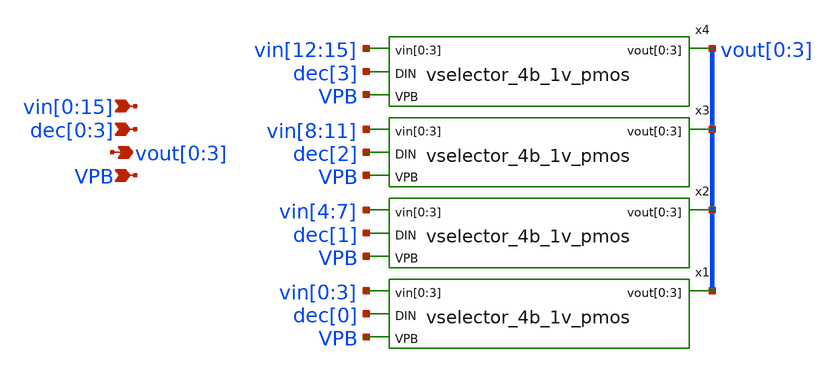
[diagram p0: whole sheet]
** sch_path: xschem/vselector_6b_1v_stage_2_pmos.sch
**.subckt vselector_6b_1v_stage_2_pmos
*+ vin[0],vin[1],vin[2],vin[3],vin[4],vin[5],vin[6],vin[7],vin[8],vin[9],vin[10],vin[11],vin[12],vin[13],vin[14],vin[15] vout[0],vout[1],vout[2],vout[3] VPB dec[0],dec[1],dec[2],dec[3]
*.ipin
*+ vin[0],vin[1],vin[2],vin[3],vin[4],vin[5],vin[6],vin[7],vin[8],vin[9],vin[10],vin[11],vin[12],vin[13],vin[14],vin[15]
*.opin vout[0],vout[1],vout[2],vout[3]
*.ipin VPB
*.ipin dec[0],dec[1],dec[2],dec[3]
x1 vin[0] vin[1] vin[2] vin[3] dec[0] vout[0] vout[1] vout[2] vout[3] VPB vselector_4b_1v_pmos
x2 vin[4] vin[5] vin[6] vin[7] dec[1] vout[0] vout[1] vout[2] vout[3] VPB vselector_4b_1v_pmos
x3 vin[8] vin[9] vin[10] vin[11] dec[2] vout[0] vout[1] vout[2] vout[3] VPB vselector_4b_1v_pmos
x4 vin[12] vin[13] vin[14] vin[15] dec[3] vout[0] vout[1] vout[2] vout[3] VPB vselector_4b_1v_pmos
**.ends

* expanding   symbol:  vselector_4b_1v_pmos.sym # of pins=4
** sym_path: xschem/vselector_4b_1v_pmos.sym
** sch_path: xschem/vselector_4b_1v_pmos.sch
.subckt vselector_4b_1v_pmos vin[0] vin[1] vin[2] vin[3] DIN vout[0] vout[1] vout[2] vout[3] VPB
*.ipin vin[0],vin[1],vin[2],vin[3]
*.opin vout[0],vout[1],vout[2],vout[3]
*.ipin VPB
*.ipin DIN
.param wp=0.42 wn=0.42 l=0.5

XM1 vout[0] DIN vin[0] VPB sky130_fd_pr__pfet_g5v0d10v5 L=l W=wp nf=1 ad='int((nf+1)/2) * W/nf * 0.29'
+ as='int((nf+2)/2) * W/nf * 0.29' pd='2*int((nf+1)/2) * (W/nf + 0.29)' ps='2*int((nf+2)/2) * (W/nf + 0.29)'
+ nrd='0.29 / W' nrs='0.29 / W' sa=0 sb=0 sd=0 mult=1 m=1
XM2 vout[1] DIN vin[1] VPB sky130_fd_pr__pfet_g5v0d10v5 L=l W=wp nf=1 ad='int((nf+1)/2) * W/nf * 0.29'
+ as='int((nf+2)/2) * W/nf * 0.29' pd='2*int((nf+1)/2) * (W/nf + 0.29)' ps='2*int((nf+2)/2) * (W/nf + 0.29)'
+ nrd='0.29 / W' nrs='0.29 / W' sa=0 sb=0 sd=0 mult=1 m=1
XM3 vout[2] DIN vin[2] VPB sky130_fd_pr__pfet_g5v0d10v5 L=l W=wp nf=1 ad='int((nf+1)/2) * W/nf * 0.29'
+ as='int((nf+2)/2) * W/nf * 0.29' pd='2*int((nf+1)/2) * (W/nf + 0.29)' ps='2*int((nf+2)/2) * (W/nf + 0.29)'
+ nrd='0.29 / W' nrs='0.29 / W' sa=0 sb=0 sd=0 mult=1 m=1
XM4 vout[3] DIN vin[3] VPB sky130_fd_pr__pfet_g5v0d10v5 L=l W=wp nf=1 ad='int((nf+1)/2) * W/nf * 0.29'
+ as='int((nf+2)/2) * W/nf * 0.29' pd='2*int((nf+1)/2) * (W/nf + 0.29)' ps='2*int((nf+2)/2) * (W/nf + 0.29)'
+ nrd='0.29 / W' nrs='0.29 / W' sa=0 sb=0 sd=0 mult=1 m=1
.ends

.end
